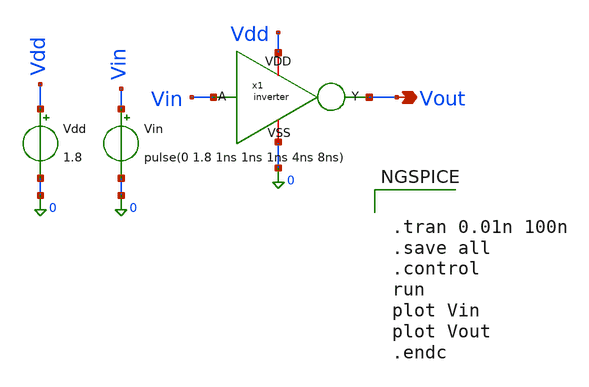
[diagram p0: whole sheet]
** sch_path: Familiarisation of IIC-OSIC-TOOLS/Test Bench/Transient/inverter_tb_tran.sch
**.subckt inverter_tb_tran Vout
*.opin Vout
x1 Vdd Vin Vout 0 inverter
Vin Vin 0 pulse(0 1.8 1ns 1ns 1ns 4ns 8ns)
Vdd Vdd 0 1.8
**** begin user architecture code

** opencircuitdesign pdks install
.lib $::SKYWATER_MODELS/sky130.lib.spice tt



.tran 0.01n 100n
.save all
.control
run
plot Vin
plot Vout
.endc


**** end user architecture code
**.ends
.end
